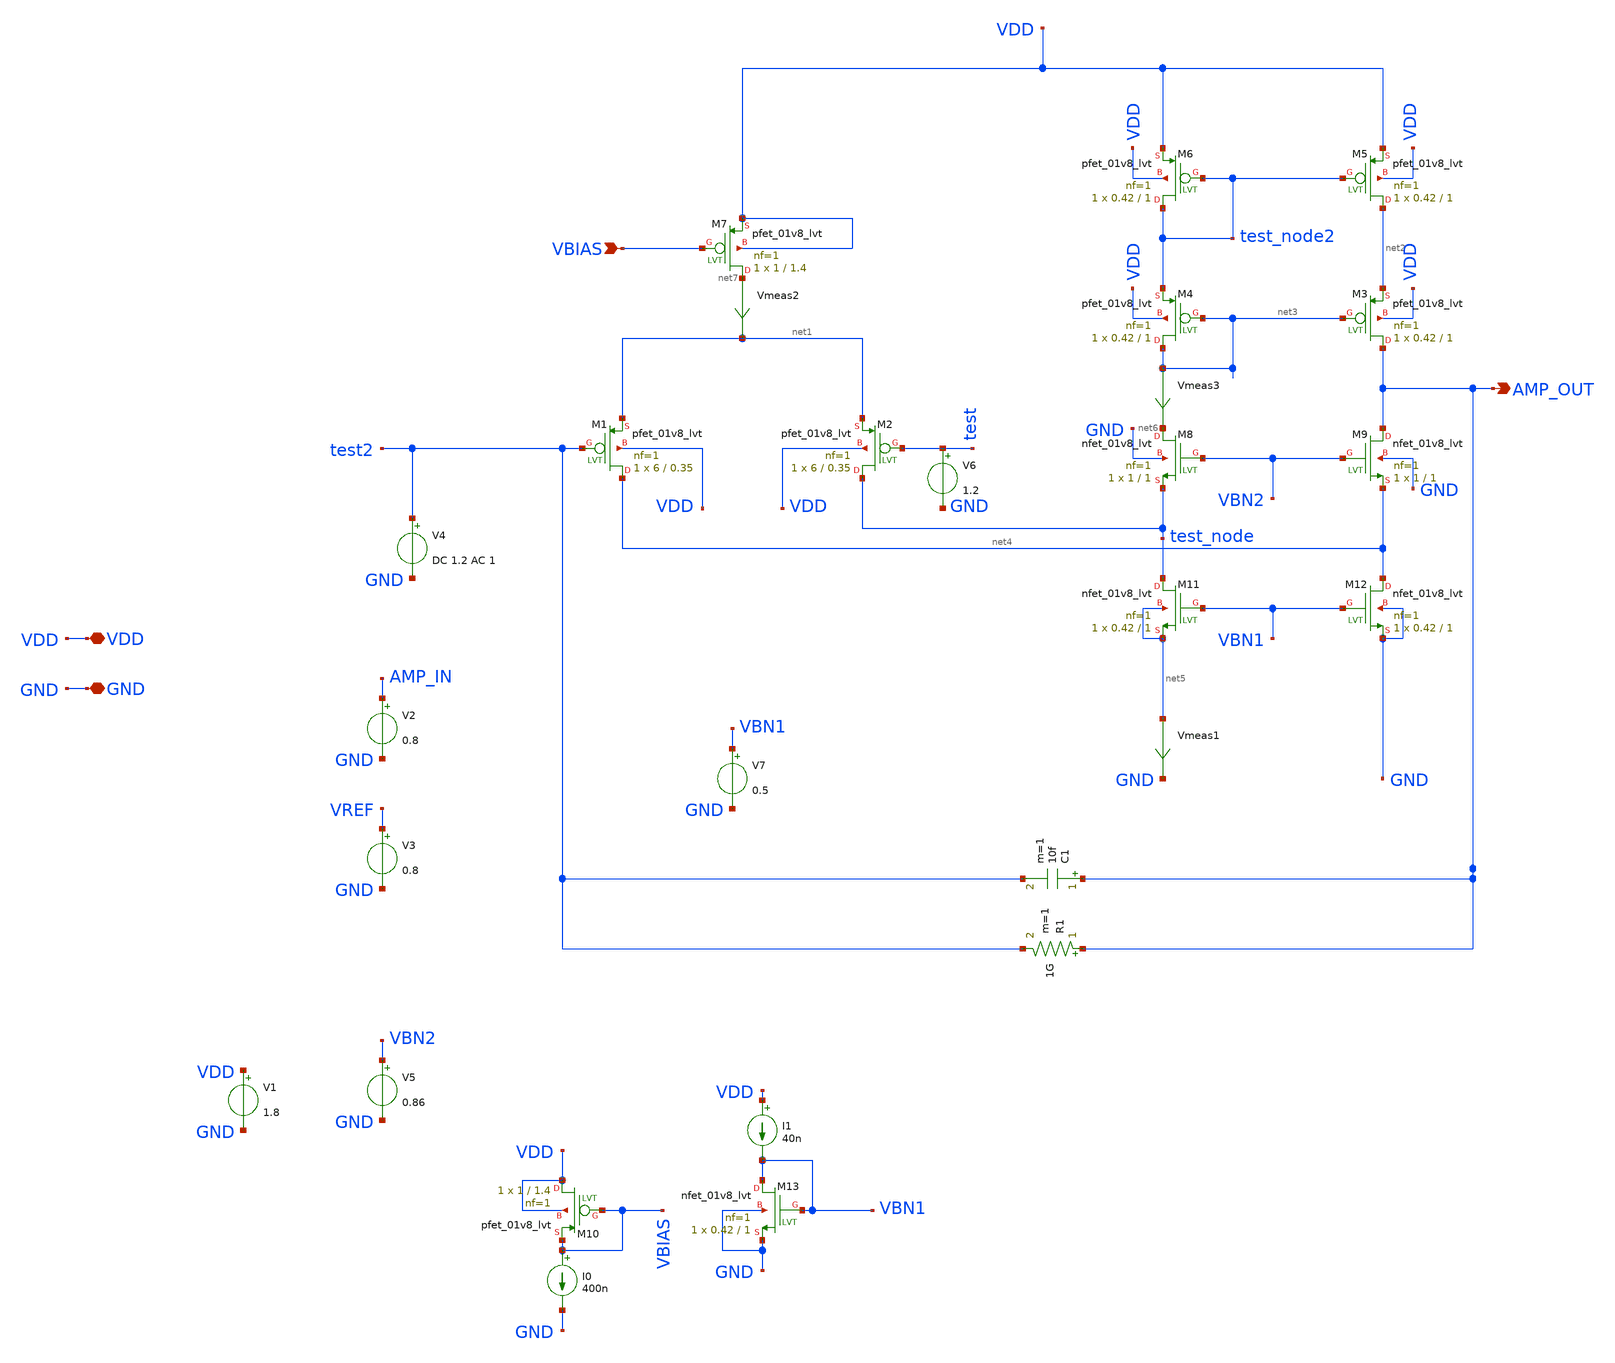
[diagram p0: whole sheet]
** sch_path: xschem/testbench/pmos_fcs.sch
**.subckt pmos_fcs AMP_OUT VBIAS VDD GND
*.opin AMP_OUT
*.ipin VBIAS
*.iopin VDD
*.iopin GND
XM1 net4 test2 net1 VDD sky130_fd_pr__pfet_01v8_lvt L=0.35 W=6 nf=1 ad='int((nf+1)/2) * W/nf * 0.29'
+ as='int((nf+2)/2) * W/nf * 0.29' pd='2*int((nf+1)/2) * (W/nf + 0.29)' ps='2*int((nf+2)/2) * (W/nf + 0.29)'
+ nrd='0.29 / W' nrs='0.29 / W' sa=0 sb=0 sd=0 mult=1 m=1
XM2 test_node test net1 VDD sky130_fd_pr__pfet_01v8_lvt L=0.35 W=6 nf=1 ad='int((nf+1)/2) * W/nf * 0.29'
+ as='int((nf+2)/2) * W/nf * 0.29' pd='2*int((nf+1)/2) * (W/nf + 0.29)' ps='2*int((nf+2)/2) * (W/nf + 0.29)'
+ nrd='0.29 / W' nrs='0.29 / W' sa=0 sb=0 sd=0 mult=1 m=1
XM5 net2 test_node2 VDD VDD sky130_fd_pr__pfet_01v8_lvt L=1 W=0.42 nf=1 ad='int((nf+1)/2) * W/nf * 0.29'
+ as='int((nf+2)/2) * W/nf * 0.29' pd='2*int((nf+1)/2) * (W/nf + 0.29)' ps='2*int((nf+2)/2) * (W/nf + 0.29)'
+ nrd='0.29 / W' nrs='0.29 / W' sa=0 sb=0 sd=0 mult=1 m=1
XM6 test_node2 test_node2 VDD VDD sky130_fd_pr__pfet_01v8_lvt L=1 W=0.42 nf=1 ad='int((nf+1)/2) * W/nf * 0.29'
+ as='int((nf+2)/2) * W/nf * 0.29' pd='2*int((nf+1)/2) * (W/nf + 0.29)' ps='2*int((nf+2)/2) * (W/nf + 0.29)'
+ nrd='0.29 / W' nrs='0.29 / W' sa=0 sb=0 sd=0 mult=1 m=1
XM3 AMP_OUT net3 net2 VDD sky130_fd_pr__pfet_01v8_lvt L=1 W=0.42 nf=1 ad='int((nf+1)/2) * W/nf * 0.29'
+ as='int((nf+2)/2) * W/nf * 0.29' pd='2*int((nf+1)/2) * (W/nf + 0.29)' ps='2*int((nf+2)/2) * (W/nf + 0.29)'
+ nrd='0.29 / W' nrs='0.29 / W' sa=0 sb=0 sd=0 mult=1 m=1
XM4 net3 net3 test_node2 VDD sky130_fd_pr__pfet_01v8_lvt L=1 W=0.42 nf=1 ad='int((nf+1)/2) * W/nf * 0.29'
+ as='int((nf+2)/2) * W/nf * 0.29' pd='2*int((nf+1)/2) * (W/nf + 0.29)' ps='2*int((nf+2)/2) * (W/nf + 0.29)'
+ nrd='0.29 / W' nrs='0.29 / W' sa=0 sb=0 sd=0 mult=1 m=1
XM8 net6 VBN2 test_node GND sky130_fd_pr__nfet_01v8_lvt L=1 W=1 nf=1 ad='int((nf+1)/2) * W/nf * 0.29'
+ as='int((nf+2)/2) * W/nf * 0.29' pd='2*int((nf+1)/2) * (W/nf + 0.29)' ps='2*int((nf+2)/2) * (W/nf + 0.29)'
+ nrd='0.29 / W' nrs='0.29 / W' sa=0 sb=0 sd=0 mult=1 m=1
XM9 AMP_OUT VBN2 net4 GND sky130_fd_pr__nfet_01v8_lvt L=1 W=1 nf=1 ad='int((nf+1)/2) * W/nf * 0.29' as='int((nf+2)/2) * W/nf * 0.29'
+ pd='2*int((nf+1)/2) * (W/nf + 0.29)' ps='2*int((nf+2)/2) * (W/nf + 0.29)' nrd='0.29 / W' nrs='0.29 / W'
+ sa=0 sb=0 sd=0 mult=1 m=1
XM7 net7 VBIAS VDD VDD sky130_fd_pr__pfet_01v8_lvt L=1.4 W=1 nf=1 ad='int((nf+1)/2) * W/nf * 0.29' as='int((nf+2)/2) * W/nf * 0.29'
+ pd='2*int((nf+1)/2) * (W/nf + 0.29)' ps='2*int((nf+2)/2) * (W/nf + 0.29)' nrd='0.29 / W' nrs='0.29 / W'
+ sa=0 sb=0 sd=0 mult=1 m=1
XM11 test_node VBN1 net5 net5 sky130_fd_pr__nfet_01v8_lvt L=1 W=0.42 nf=1 ad='int((nf+1)/2) * W/nf * 0.29'
+ as='int((nf+2)/2) * W/nf * 0.29' pd='2*int((nf+1)/2) * (W/nf + 0.29)' ps='2*int((nf+2)/2) * (W/nf + 0.29)'
+ nrd='0.29 / W' nrs='0.29 / W' sa=0 sb=0 sd=0 mult=1 m=1
XM12 net4 VBN1 GND GND sky130_fd_pr__nfet_01v8_lvt L=1 W=0.42 nf=1 ad='int((nf+1)/2) * W/nf * 0.29' as='int((nf+2)/2) * W/nf * 0.29'
+ pd='2*int((nf+1)/2) * (W/nf + 0.29)' ps='2*int((nf+2)/2) * (W/nf + 0.29)' nrd='0.29 / W' nrs='0.29 / W'
+ sa=0 sb=0 sd=0 mult=1 m=1
V2 AMP_IN GND 0.8
V3 VREF GND 0.8
V5 VBN2 GND 0.86
XM10 VDD VBIAS VBIAS VDD sky130_fd_pr__pfet_01v8_lvt L=1.4 W=1 nf=1 ad='int((nf+1)/2) * W/nf * 0.29'
+ as='int((nf+2)/2) * W/nf * 0.29' pd='2*int((nf+1)/2) * (W/nf + 0.29)' ps='2*int((nf+2)/2) * (W/nf + 0.29)'
+ nrd='0.29 / W' nrs='0.29 / W' sa=0 sb=0 sd=0 mult=1 m=1
V1 VDD GND 1.8
I0 VBIAS GND 400n
XM13 VBN1 VBN1 GND GND sky130_fd_pr__nfet_01v8_lvt L=1 W=0.42 nf=1 ad='int((nf+1)/2) * W/nf * 0.29' as='int((nf+2)/2) * W/nf * 0.29'
+ pd='2*int((nf+1)/2) * (W/nf + 0.29)' ps='2*int((nf+2)/2) * (W/nf + 0.29)' nrd='0.29 / W' nrs='0.29 / W'
+ sa=0 sb=0 sd=0 mult=1 m=1
I1 VDD VBN1 40n
Vmeas1 net5 GND 0
.save i(vmeas1)
Vmeas2 net7 net1 0
.save i(vmeas2)
V4 test2 GND DC 1.2 AC 1
V6 test GND 1.2
Vmeas3 net3 net6 0
.save i(vmeas3)
C1 AMP_OUT test2 10f m=1
R1 AMP_OUT test2 1G m=1
V7 VBN1 GND 0.5
**** begin user architecture code

** opencircuitdesign pdks install
.lib $::SKYWATER_MODELS/sky130.lib.spice tt


**** end user architecture code
**.ends
**** begin user architecture code


.options gmin=0.0000000000000000000001
*.options savecurrents

.control
save all

*tran 1m 50m
*plot v(test)
*op
*dc v4 1 1.4 0.0001
ac dec 10 1 1000Meg
plot vdb(AMP_OUT) 180*cph(v(AMP_OUT))/pi xlog

*plot v(AMP_OUT)
*plot deriv(v(AMP_OUT))

*noise v(AMP_OUT) V4 dec 10 1 1Meg
*setplot noise2
*print onoise_total

*noise v(PIX_OUT) V8 dec 10 1 1Meg
*setplot noise2
*print onoise_total
.endc


**** end user architecture code
.end
